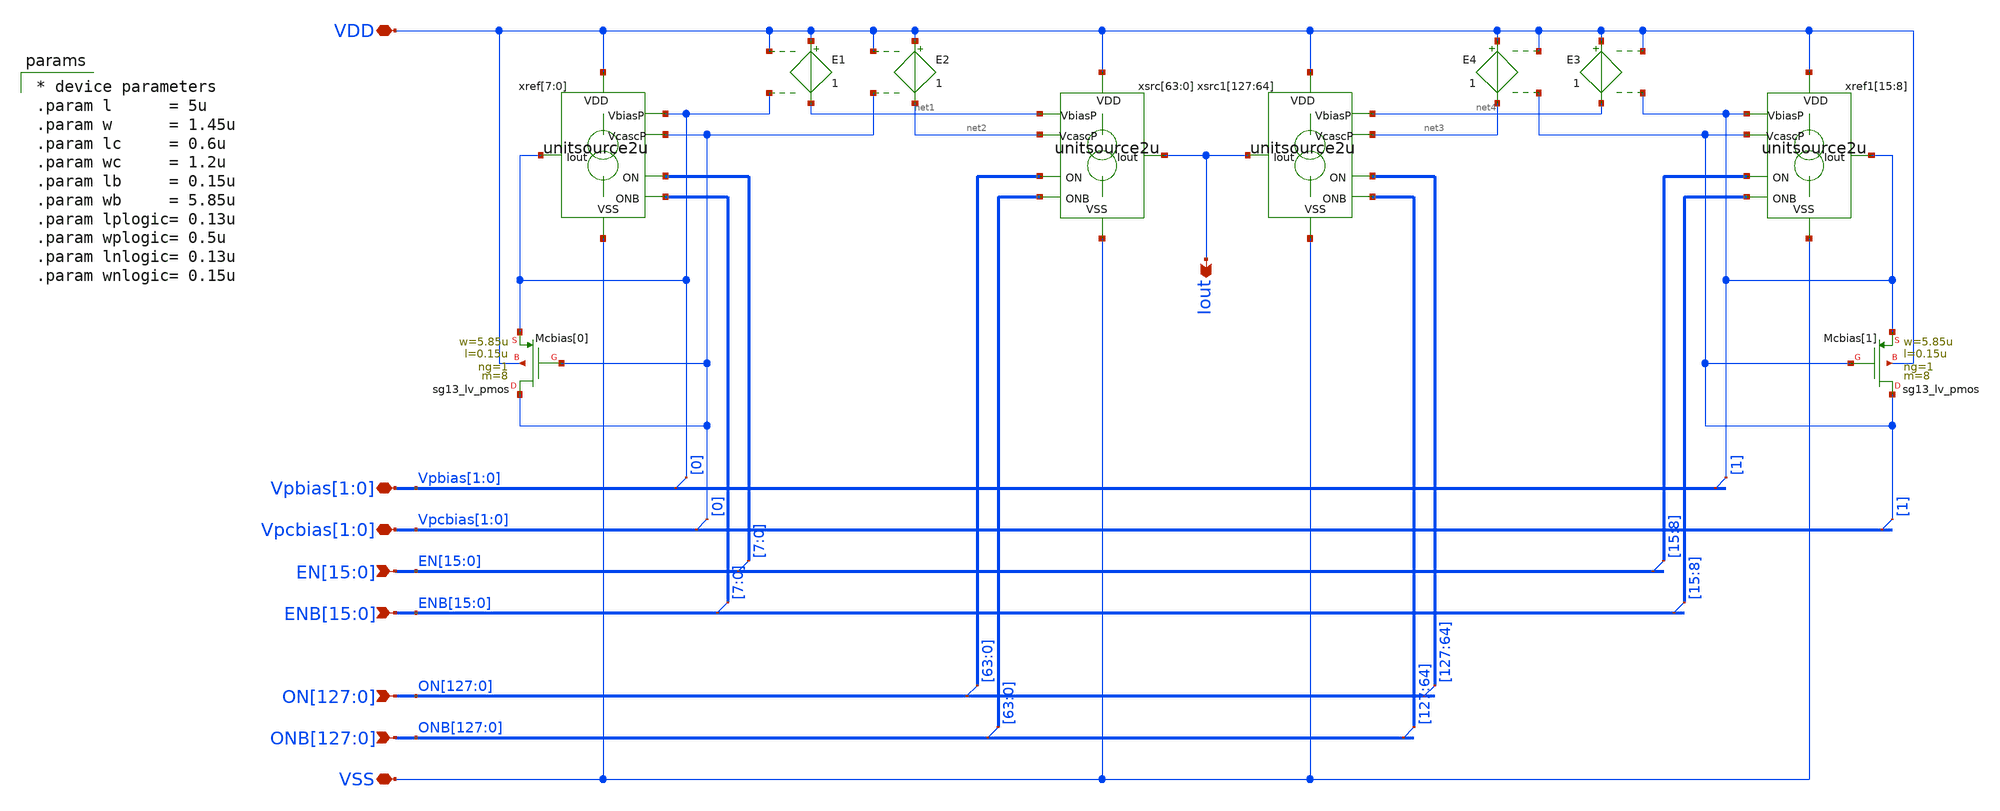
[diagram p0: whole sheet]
** sch_path: xschem/dac128module.sch
**.subckt dac128module Iout
*+ ON[127],ON[126],ON[125],ON[124],ON[123],ON[122],ON[121],ON[120],ON[119],ON[118],ON[117],ON[116],ON[115],ON[114],ON[113],ON[112],ON[111],ON[110],ON[109],ON[108],ON[107],ON[106],ON[105],ON[104],ON[103],ON[102],ON[101],ON[100],ON[99],ON[98],ON[97],ON[96],ON[95],ON[94],ON[93],ON[92],ON[91],ON[90],ON[89],ON[88],ON[87],ON[86],ON[85],ON[84],ON[83],ON[82],ON[81],ON[80],ON[79],ON[78],ON[77],ON[76],ON[75],ON[74],ON[73],ON[72],ON[71],ON[70],ON[69],ON[68],ON[67],ON[66],ON[65],ON[64],ON[63],ON[62],ON[61],ON[60],ON[59],ON[58],ON[57],ON[56],ON[55],ON[54],ON[53],ON[52],ON[51],ON[50],ON[49],ON[48],ON[47],ON[46],ON[45],ON[44],ON[43],ON[42],ON[41],ON[40],ON[39],ON[38],ON[37],ON[36],ON[35],ON[34],ON[33],ON[32],ON[31],ON[30],ON[29],ON[28],ON[27],ON[26],ON[25],ON[24],ON[23],ON[22],ON[21],ON[20],ON[19],ON[18],ON[17],ON[16],ON[15],ON[14],ON[13],ON[12],ON[11],ON[10],ON[9],ON[8],ON[7],ON[6],ON[5],ON[4],ON[3],ON[2],ON[1],ON[0]
*+ ONB[127],ONB[126],ONB[125],ONB[124],ONB[123],ONB[122],ONB[121],ONB[120],ONB[119],ONB[118],ONB[117],ONB[116],ONB[115],ONB[114],ONB[113],ONB[112],ONB[111],ONB[110],ONB[109],ONB[108],ONB[107],ONB[106],ONB[105],ONB[104],ONB[103],ONB[102],ONB[101],ONB[100],ONB[99],ONB[98],ONB[97],ONB[96],ONB[95],ONB[94],ONB[93],ONB[92],ONB[91],ONB[90],ONB[89],ONB[88],ONB[87],ONB[86],ONB[85],ONB[84],ONB[83],ONB[82],ONB[81],ONB[80],ONB[79],ONB[78],ONB[77],ONB[76],ONB[75],ONB[74],ONB[73],ONB[72],ONB[71],ONB[70],ONB[69],ONB[68],ONB[67],ONB[66],ONB[65],ONB[64],ONB[63],ONB[62],ONB[61],ONB[60],ONB[59],ONB[58],ONB[57],ONB[56],ONB[55],ONB[54],ONB[53],ONB[52],ONB[51],ONB[50],ONB[49],ONB[48],ONB[47],ONB[46],ONB[45],ONB[44],ONB[43],ONB[42],ONB[41],ONB[40],ONB[39],ONB[38],ONB[37],ONB[36],ONB[35],ONB[34],ONB[33],ONB[32],ONB[31],ONB[30],ONB[29],ONB[28],ONB[27],ONB[26],ONB[25],ONB[24],ONB[23],ONB[22],ONB[21],ONB[20],ONB[19],ONB[18],ONB[17],ONB[16],ONB[15],ONB[14],ONB[13],ONB[12],ONB[11],ONB[10],ONB[9],ONB[8],ONB[7],ONB[6],ONB[5],ONB[4],ONB[3],ONB[2],ONB[1],ONB[0] VSS VDD Vpcbias[1],Vpcbias[0]
*+ EN[15],EN[14],EN[13],EN[12],EN[11],EN[10],EN[9],EN[8],EN[7],EN[6],EN[5],EN[4],EN[3],EN[2],EN[1],EN[0]
*+ ENB[15],ENB[14],ENB[13],ENB[12],ENB[11],ENB[10],ENB[9],ENB[8],ENB[7],ENB[6],ENB[5],ENB[4],ENB[3],ENB[2],ENB[1],ENB[0] Vpbias[1],Vpbias[0]
*.opin Iout
*.ipin
*+ ON[127],ON[126],ON[125],ON[124],ON[123],ON[122],ON[121],ON[120],ON[119],ON[118],ON[117],ON[116],ON[115],ON[114],ON[113],ON[112],ON[111],ON[110],ON[109],ON[108],ON[107],ON[106],ON[105],ON[104],ON[103],ON[102],ON[101],ON[100],ON[99],ON[98],ON[97],ON[96],ON[95],ON[94],ON[93],ON[92],ON[91],ON[90],ON[89],ON[88],ON[87],ON[86],ON[85],ON[84],ON[83],ON[82],ON[81],ON[80],ON[79],ON[78],ON[77],ON[76],ON[75],ON[74],ON[73],ON[72],ON[71],ON[70],ON[69],ON[68],ON[67],ON[66],ON[65],ON[64],ON[63],ON[62],ON[61],ON[60],ON[59],ON[58],ON[57],ON[56],ON[55],ON[54],ON[53],ON[52],ON[51],ON[50],ON[49],ON[48],ON[47],ON[46],ON[45],ON[44],ON[43],ON[42],ON[41],ON[40],ON[39],ON[38],ON[37],ON[36],ON[35],ON[34],ON[33],ON[32],ON[31],ON[30],ON[29],ON[28],ON[27],ON[26],ON[25],ON[24],ON[23],ON[22],ON[21],ON[20],ON[19],ON[18],ON[17],ON[16],ON[15],ON[14],ON[13],ON[12],ON[11],ON[10],ON[9],ON[8],ON[7],ON[6],ON[5],ON[4],ON[3],ON[2],ON[1],ON[0]
*.ipin
*+ ONB[127],ONB[126],ONB[125],ONB[124],ONB[123],ONB[122],ONB[121],ONB[120],ONB[119],ONB[118],ONB[117],ONB[116],ONB[115],ONB[114],ONB[113],ONB[112],ONB[111],ONB[110],ONB[109],ONB[108],ONB[107],ONB[106],ONB[105],ONB[104],ONB[103],ONB[102],ONB[101],ONB[100],ONB[99],ONB[98],ONB[97],ONB[96],ONB[95],ONB[94],ONB[93],ONB[92],ONB[91],ONB[90],ONB[89],ONB[88],ONB[87],ONB[86],ONB[85],ONB[84],ONB[83],ONB[82],ONB[81],ONB[80],ONB[79],ONB[78],ONB[77],ONB[76],ONB[75],ONB[74],ONB[73],ONB[72],ONB[71],ONB[70],ONB[69],ONB[68],ONB[67],ONB[66],ONB[65],ONB[64],ONB[63],ONB[62],ONB[61],ONB[60],ONB[59],ONB[58],ONB[57],ONB[56],ONB[55],ONB[54],ONB[53],ONB[52],ONB[51],ONB[50],ONB[49],ONB[48],ONB[47],ONB[46],ONB[45],ONB[44],ONB[43],ONB[42],ONB[41],ONB[40],ONB[39],ONB[38],ONB[37],ONB[36],ONB[35],ONB[34],ONB[33],ONB[32],ONB[31],ONB[30],ONB[29],ONB[28],ONB[27],ONB[26],ONB[25],ONB[24],ONB[23],ONB[22],ONB[21],ONB[20],ONB[19],ONB[18],ONB[17],ONB[16],ONB[15],ONB[14],ONB[13],ONB[12],ONB[11],ONB[10],ONB[9],ONB[8],ONB[7],ONB[6],ONB[5],ONB[4],ONB[3],ONB[2],ONB[1],ONB[0]
*.iopin VSS
*.iopin VDD
*.iopin Vpcbias[1],Vpcbias[0]
*.ipin
*+ EN[15],EN[14],EN[13],EN[12],EN[11],EN[10],EN[9],EN[8],EN[7],EN[6],EN[5],EN[4],EN[3],EN[2],EN[1],EN[0]
*.ipin
*+ ENB[15],ENB[14],ENB[13],ENB[12],ENB[11],ENB[10],ENB[9],ENB[8],ENB[7],ENB[6],ENB[5],ENB[4],ENB[3],ENB[2],ENB[1],ENB[0]
*.iopin Vpbias[1],Vpbias[0]
XMcbias[0] Vpcbias[0] Vpcbias[0] Vpbias[0] VDD sg13_lv_pmos w=5.85u l=0.15u ng=1 m=8 mm_ok=1
xref[7] VDD Vpbias[0] EN[7] ENB[7] Vpbias[0] Vpcbias[0] VSS unitsource2u
xref[6] VDD Vpbias[0] EN[6] ENB[6] Vpbias[0] Vpcbias[0] VSS unitsource2u
xref[5] VDD Vpbias[0] EN[5] ENB[5] Vpbias[0] Vpcbias[0] VSS unitsource2u
xref[4] VDD Vpbias[0] EN[4] ENB[4] Vpbias[0] Vpcbias[0] VSS unitsource2u
xref[3] VDD Vpbias[0] EN[3] ENB[3] Vpbias[0] Vpcbias[0] VSS unitsource2u
xref[2] VDD Vpbias[0] EN[2] ENB[2] Vpbias[0] Vpcbias[0] VSS unitsource2u
xref[1] VDD Vpbias[0] EN[1] ENB[1] Vpbias[0] Vpcbias[0] VSS unitsource2u
xref[0] VDD Vpbias[0] EN[0] ENB[0] Vpbias[0] Vpcbias[0] VSS unitsource2u
xsrc[63] VDD net1 ON[63] ONB[63] Iout net2 VSS unitsource2u
xsrc[62] VDD net1 ON[62] ONB[62] Iout net2 VSS unitsource2u
xsrc[61] VDD net1 ON[61] ONB[61] Iout net2 VSS unitsource2u
xsrc[60] VDD net1 ON[60] ONB[60] Iout net2 VSS unitsource2u
xsrc[59] VDD net1 ON[59] ONB[59] Iout net2 VSS unitsource2u
xsrc[58] VDD net1 ON[58] ONB[58] Iout net2 VSS unitsource2u
xsrc[57] VDD net1 ON[57] ONB[57] Iout net2 VSS unitsource2u
xsrc[56] VDD net1 ON[56] ONB[56] Iout net2 VSS unitsource2u
xsrc[55] VDD net1 ON[55] ONB[55] Iout net2 VSS unitsource2u
xsrc[54] VDD net1 ON[54] ONB[54] Iout net2 VSS unitsource2u
xsrc[53] VDD net1 ON[53] ONB[53] Iout net2 VSS unitsource2u
xsrc[52] VDD net1 ON[52] ONB[52] Iout net2 VSS unitsource2u
xsrc[51] VDD net1 ON[51] ONB[51] Iout net2 VSS unitsource2u
xsrc[50] VDD net1 ON[50] ONB[50] Iout net2 VSS unitsource2u
xsrc[49] VDD net1 ON[49] ONB[49] Iout net2 VSS unitsource2u
xsrc[48] VDD net1 ON[48] ONB[48] Iout net2 VSS unitsource2u
xsrc[47] VDD net1 ON[47] ONB[47] Iout net2 VSS unitsource2u
xsrc[46] VDD net1 ON[46] ONB[46] Iout net2 VSS unitsource2u
xsrc[45] VDD net1 ON[45] ONB[45] Iout net2 VSS unitsource2u
xsrc[44] VDD net1 ON[44] ONB[44] Iout net2 VSS unitsource2u
xsrc[43] VDD net1 ON[43] ONB[43] Iout net2 VSS unitsource2u
xsrc[42] VDD net1 ON[42] ONB[42] Iout net2 VSS unitsource2u
xsrc[41] VDD net1 ON[41] ONB[41] Iout net2 VSS unitsource2u
xsrc[40] VDD net1 ON[40] ONB[40] Iout net2 VSS unitsource2u
xsrc[39] VDD net1 ON[39] ONB[39] Iout net2 VSS unitsource2u
xsrc[38] VDD net1 ON[38] ONB[38] Iout net2 VSS unitsource2u
xsrc[37] VDD net1 ON[37] ONB[37] Iout net2 VSS unitsource2u
xsrc[36] VDD net1 ON[36] ONB[36] Iout net2 VSS unitsource2u
xsrc[35] VDD net1 ON[35] ONB[35] Iout net2 VSS unitsource2u
xsrc[34] VDD net1 ON[34] ONB[34] Iout net2 VSS unitsource2u
xsrc[33] VDD net1 ON[33] ONB[33] Iout net2 VSS unitsource2u
xsrc[32] VDD net1 ON[32] ONB[32] Iout net2 VSS unitsource2u
xsrc[31] VDD net1 ON[31] ONB[31] Iout net2 VSS unitsource2u
xsrc[30] VDD net1 ON[30] ONB[30] Iout net2 VSS unitsource2u
xsrc[29] VDD net1 ON[29] ONB[29] Iout net2 VSS unitsource2u
xsrc[28] VDD net1 ON[28] ONB[28] Iout net2 VSS unitsource2u
xsrc[27] VDD net1 ON[27] ONB[27] Iout net2 VSS unitsource2u
xsrc[26] VDD net1 ON[26] ONB[26] Iout net2 VSS unitsource2u
xsrc[25] VDD net1 ON[25] ONB[25] Iout net2 VSS unitsource2u
xsrc[24] VDD net1 ON[24] ONB[24] Iout net2 VSS unitsource2u
xsrc[23] VDD net1 ON[23] ONB[23] Iout net2 VSS unitsource2u
xsrc[22] VDD net1 ON[22] ONB[22] Iout net2 VSS unitsource2u
xsrc[21] VDD net1 ON[21] ONB[21] Iout net2 VSS unitsource2u
xsrc[20] VDD net1 ON[20] ONB[20] Iout net2 VSS unitsource2u
xsrc[19] VDD net1 ON[19] ONB[19] Iout net2 VSS unitsource2u
xsrc[18] VDD net1 ON[18] ONB[18] Iout net2 VSS unitsource2u
xsrc[17] VDD net1 ON[17] ONB[17] Iout net2 VSS unitsource2u
xsrc[16] VDD net1 ON[16] ONB[16] Iout net2 VSS unitsource2u
xsrc[15] VDD net1 ON[15] ONB[15] Iout net2 VSS unitsource2u
xsrc[14] VDD net1 ON[14] ONB[14] Iout net2 VSS unitsource2u
xsrc[13] VDD net1 ON[13] ONB[13] Iout net2 VSS unitsource2u
xsrc[12] VDD net1 ON[12] ONB[12] Iout net2 VSS unitsource2u
xsrc[11] VDD net1 ON[11] ONB[11] Iout net2 VSS unitsource2u
xsrc[10] VDD net1 ON[10] ONB[10] Iout net2 VSS unitsource2u
xsrc[9] VDD net1 ON[9] ONB[9] Iout net2 VSS unitsource2u
xsrc[8] VDD net1 ON[8] ONB[8] Iout net2 VSS unitsource2u
xsrc[7] VDD net1 ON[7] ONB[7] Iout net2 VSS unitsource2u
xsrc[6] VDD net1 ON[6] ONB[6] Iout net2 VSS unitsource2u
xsrc[5] VDD net1 ON[5] ONB[5] Iout net2 VSS unitsource2u
xsrc[4] VDD net1 ON[4] ONB[4] Iout net2 VSS unitsource2u
xsrc[3] VDD net1 ON[3] ONB[3] Iout net2 VSS unitsource2u
xsrc[2] VDD net1 ON[2] ONB[2] Iout net2 VSS unitsource2u
xsrc[1] VDD net1 ON[1] ONB[1] Iout net2 VSS unitsource2u
xsrc[0] VDD net1 ON[0] ONB[0] Iout net2 VSS unitsource2u
XMcbias[1] Vpcbias[1] Vpcbias[1] Vpbias[1] VDD sg13_lv_pmos w=5.85u l=0.15u ng=1 m=8 mm_ok=1
xref1[15] VDD Vpbias[1] EN[15] ENB[15] Vpbias[1] Vpcbias[1] VSS unitsource2u
xref1[14] VDD Vpbias[1] EN[14] ENB[14] Vpbias[1] Vpcbias[1] VSS unitsource2u
xref1[13] VDD Vpbias[1] EN[13] ENB[13] Vpbias[1] Vpcbias[1] VSS unitsource2u
xref1[12] VDD Vpbias[1] EN[12] ENB[12] Vpbias[1] Vpcbias[1] VSS unitsource2u
xref1[11] VDD Vpbias[1] EN[11] ENB[11] Vpbias[1] Vpcbias[1] VSS unitsource2u
xref1[10] VDD Vpbias[1] EN[10] ENB[10] Vpbias[1] Vpcbias[1] VSS unitsource2u
xref1[9] VDD Vpbias[1] EN[9] ENB[9] Vpbias[1] Vpcbias[1] VSS unitsource2u
xref1[8] VDD Vpbias[1] EN[8] ENB[8] Vpbias[1] Vpcbias[1] VSS unitsource2u
xsrc1[127] VDD net4 ON[127] ONB[127] Iout net3 VSS unitsource2u
xsrc1[126] VDD net4 ON[126] ONB[126] Iout net3 VSS unitsource2u
xsrc1[125] VDD net4 ON[125] ONB[125] Iout net3 VSS unitsource2u
xsrc1[124] VDD net4 ON[124] ONB[124] Iout net3 VSS unitsource2u
xsrc1[123] VDD net4 ON[123] ONB[123] Iout net3 VSS unitsource2u
xsrc1[122] VDD net4 ON[122] ONB[122] Iout net3 VSS unitsource2u
xsrc1[121] VDD net4 ON[121] ONB[121] Iout net3 VSS unitsource2u
xsrc1[120] VDD net4 ON[120] ONB[120] Iout net3 VSS unitsource2u
xsrc1[119] VDD net4 ON[119] ONB[119] Iout net3 VSS unitsource2u
xsrc1[118] VDD net4 ON[118] ONB[118] Iout net3 VSS unitsource2u
xsrc1[117] VDD net4 ON[117] ONB[117] Iout net3 VSS unitsource2u
xsrc1[116] VDD net4 ON[116] ONB[116] Iout net3 VSS unitsource2u
xsrc1[115] VDD net4 ON[115] ONB[115] Iout net3 VSS unitsource2u
xsrc1[114] VDD net4 ON[114] ONB[114] Iout net3 VSS unitsource2u
xsrc1[113] VDD net4 ON[113] ONB[113] Iout net3 VSS unitsource2u
xsrc1[112] VDD net4 ON[112] ONB[112] Iout net3 VSS unitsource2u
xsrc1[111] VDD net4 ON[111] ONB[111] Iout net3 VSS unitsource2u
xsrc1[110] VDD net4 ON[110] ONB[110] Iout net3 VSS unitsource2u
xsrc1[109] VDD net4 ON[109] ONB[109] Iout net3 VSS unitsource2u
xsrc1[108] VDD net4 ON[108] ONB[108] Iout net3 VSS unitsource2u
xsrc1[107] VDD net4 ON[107] ONB[107] Iout net3 VSS unitsource2u
xsrc1[106] VDD net4 ON[106] ONB[106] Iout net3 VSS unitsource2u
xsrc1[105] VDD net4 ON[105] ONB[105] Iout net3 VSS unitsource2u
xsrc1[104] VDD net4 ON[104] ONB[104] Iout net3 VSS unitsource2u
xsrc1[103] VDD net4 ON[103] ONB[103] Iout net3 VSS unitsource2u
xsrc1[102] VDD net4 ON[102] ONB[102] Iout net3 VSS unitsource2u
xsrc1[101] VDD net4 ON[101] ONB[101] Iout net3 VSS unitsource2u
xsrc1[100] VDD net4 ON[100] ONB[100] Iout net3 VSS unitsource2u
xsrc1[99] VDD net4 ON[99] ONB[99] Iout net3 VSS unitsource2u
xsrc1[98] VDD net4 ON[98] ONB[98] Iout net3 VSS unitsource2u
xsrc1[97] VDD net4 ON[97] ONB[97] Iout net3 VSS unitsource2u
xsrc1[96] VDD net4 ON[96] ONB[96] Iout net3 VSS unitsource2u
xsrc1[95] VDD net4 ON[95] ONB[95] Iout net3 VSS unitsource2u
xsrc1[94] VDD net4 ON[94] ONB[94] Iout net3 VSS unitsource2u
xsrc1[93] VDD net4 ON[93] ONB[93] Iout net3 VSS unitsource2u
xsrc1[92] VDD net4 ON[92] ONB[92] Iout net3 VSS unitsource2u
xsrc1[91] VDD net4 ON[91] ONB[91] Iout net3 VSS unitsource2u
xsrc1[90] VDD net4 ON[90] ONB[90] Iout net3 VSS unitsource2u
xsrc1[89] VDD net4 ON[89] ONB[89] Iout net3 VSS unitsource2u
xsrc1[88] VDD net4 ON[88] ONB[88] Iout net3 VSS unitsource2u
xsrc1[87] VDD net4 ON[87] ONB[87] Iout net3 VSS unitsource2u
xsrc1[86] VDD net4 ON[86] ONB[86] Iout net3 VSS unitsource2u
xsrc1[85] VDD net4 ON[85] ONB[85] Iout net3 VSS unitsource2u
xsrc1[84] VDD net4 ON[84] ONB[84] Iout net3 VSS unitsource2u
xsrc1[83] VDD net4 ON[83] ONB[83] Iout net3 VSS unitsource2u
xsrc1[82] VDD net4 ON[82] ONB[82] Iout net3 VSS unitsource2u
xsrc1[81] VDD net4 ON[81] ONB[81] Iout net3 VSS unitsource2u
xsrc1[80] VDD net4 ON[80] ONB[80] Iout net3 VSS unitsource2u
xsrc1[79] VDD net4 ON[79] ONB[79] Iout net3 VSS unitsource2u
xsrc1[78] VDD net4 ON[78] ONB[78] Iout net3 VSS unitsource2u
xsrc1[77] VDD net4 ON[77] ONB[77] Iout net3 VSS unitsource2u
xsrc1[76] VDD net4 ON[76] ONB[76] Iout net3 VSS unitsource2u
xsrc1[75] VDD net4 ON[75] ONB[75] Iout net3 VSS unitsource2u
xsrc1[74] VDD net4 ON[74] ONB[74] Iout net3 VSS unitsource2u
xsrc1[73] VDD net4 ON[73] ONB[73] Iout net3 VSS unitsource2u
xsrc1[72] VDD net4 ON[72] ONB[72] Iout net3 VSS unitsource2u
xsrc1[71] VDD net4 ON[71] ONB[71] Iout net3 VSS unitsource2u
xsrc1[70] VDD net4 ON[70] ONB[70] Iout net3 VSS unitsource2u
xsrc1[69] VDD net4 ON[69] ONB[69] Iout net3 VSS unitsource2u
xsrc1[68] VDD net4 ON[68] ONB[68] Iout net3 VSS unitsource2u
xsrc1[67] VDD net4 ON[67] ONB[67] Iout net3 VSS unitsource2u
xsrc1[66] VDD net4 ON[66] ONB[66] Iout net3 VSS unitsource2u
xsrc1[65] VDD net4 ON[65] ONB[65] Iout net3 VSS unitsource2u
xsrc1[64] VDD net4 ON[64] ONB[64] Iout net3 VSS unitsource2u
* tap: EN[15:0] --> EN[7:0]
* tap: ENB[15:0] --> ENB[7:0]
* tap: ENB[15:0] --> ENB[15:8]
* tap: EN[15:0] --> EN[15:8]
* tap: ON[127:0] --> ON[63:0]
* tap: ONB[127:0] --> ONB[63:0]
* tap: ON[127:0] --> ON[127:64]
* tap: ONB[127:0] --> ONB[127:64]
* tap: Vpbias[1:0] --> Vpbias[0]
* tap: Vpcbias[1:0] --> Vpcbias[0]
* tap: Vpbias[1:0] --> Vpbias[1]
* tap: Vpcbias[1:0] --> Vpcbias[1]
E1 VDD net1 VDD Vpbias[0] 1
E2 VDD net2 VDD Vpcbias[0] 1
E3 VDD net4 VDD Vpbias[1] 1
E4 VDD net3 VDD Vpcbias[1] 1
**** begin user architecture code

* device parameters
.param l      = 5u
.param w      = 1.45u
.param lc     = 0.6u
.param wc     = 1.2u
.param lb     = 0.15u
.param wb     = 5.85u
.param lplogic= 0.13u
.param wplogic= 0.5u
.param lnlogic= 0.13u
.param wnlogic= 0.15u


**** end user architecture code
**.ends

* expanding   symbol:  unitsource2u.sym # of pins=7
** sym_path: xschem/unitsource2u.sym
** sch_path: xschem/unitsource2u.sch
.subckt unitsource2u VDD VbiasP ON ONB Iout VcascP VSS
*.iopin VSS
*.iopin VDD
*.iopin VbiasP
*.iopin VcascP
*.ipin ON
*.ipin ONB
*.iopin Iout
xnonoverlap VDD VSS ON ONB on_n off_n nonoverlap
xsw VDD off_n Vcasc on_n VcascP cascodeswitch_pmos
xsrc VDD VbiasP Vcasc Iout pcsource2u
.ends


* expanding   symbol:  nonoverlap.sym # of pins=6
** sym_path: xschem/nonoverlap.sym
** sch_path: xschem/nonoverlap.sch
.subckt nonoverlap VDD VSS INP INN OUTN OUTP
*.iopin VSS
*.iopin VDD
*.ipin INP
*.ipin INN
*.opin OUTP
*.opin OUTN
XM1 OUTN INP VDD VDD sg13_lv_pmos w=0.3u l=0.13u ng=1 m=1 mm_ok=1
XM2 OUTP INN VDD VDD sg13_lv_pmos w=0.3u l=0.13u ng=1 m=1 mm_ok=1
XM3 OUTN OUTP VSS VSS sg13_lv_nmos w=0.15u l=0.52u ng=1 m=1 mm_ok=1
XM4 OUTP OUTN VSS VSS sg13_lv_nmos w=0.15u l=0.52u ng=1 m=1 mm_ok=1
.ends


* expanding   symbol:  cascodeswitch_pmos.sym # of pins=5
** sym_path: xschem/cascodeswitch_pmos.sym
** sch_path: xschem/cascodeswitch_pmos.sch
.subckt cascodeswitch_pmos VDD off_n Vcasc on_n Vbpcasc
*.ipin off_n
*.ipin Vbpcasc
*.opin Vcasc
*.ipin on_n
*.ipin VDD
XMpullup Vcasc off_n VDD VDD sg13_lv_pmos w=0.3u l=0.13u ng=1 m=1 mm_ok=1
XMbias Vbpcasc on_n Vcasc VDD sg13_lv_pmos w=0.3u l=0.13u ng=1 m=1 mm_ok=1
.ends


* expanding   symbol:  pcsource2u.sym # of pins=4
** sym_path: xschem/pcsource2u.sym
** sch_path: xschem/pcsource2u.sch
.subckt pcsource2u VDD VbiasP VcascodeP Iout
*.ipin VcascodeP
*.ipin VbiasP
*.opin Iout
*.ipin VDD
XMsrc drain net4 VDD net1 sg13_lv_pmos w=1.45u l=5u ng=1 m=1 mm_ok=1
XMcasc Iout net3 drain net2 sg13_lv_pmos w=1.2u l=0.6u ng=1 m=1 mm_ok=1
Vgsrc net4 VbiasP 0
.save i(vgsrc)
Vgcasc net3 VcascodeP 0
.save i(vgcasc)
Vbsrc VDD net1 0
.save i(vbsrc)
Vbcasc VDD net2 0
.save i(vbcasc)
.ends

.end
